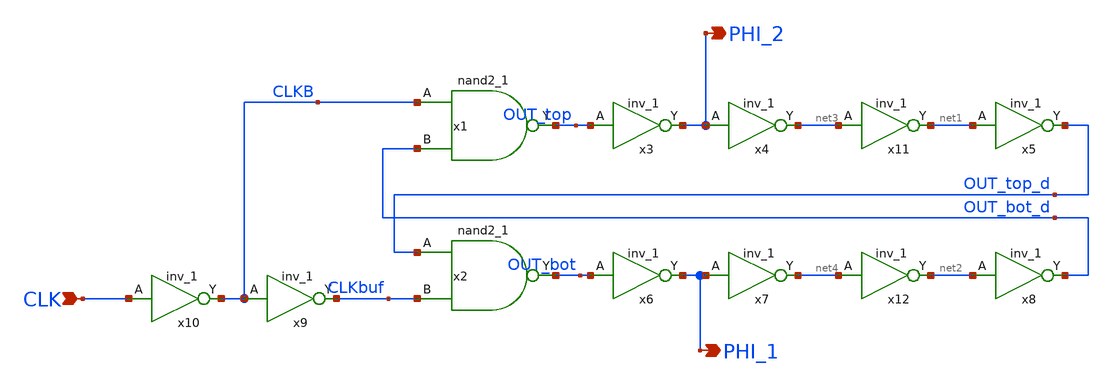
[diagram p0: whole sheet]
** sch_path: designs/switch_matrix_gf180mcu_9t5v0-main/designs/libs/core_swmatrix/NO_ClkGen.sch
**.subckt NO_ClkGen CLK PHI_2 PHI_1
*.ipin CLK
*.opin PHI_2
*.opin PHI_1
x1 CLKB OUT_bot_d VSSd VDDd VSSd VDDd OUT_top gf180mcu_fd_sc_mcu9t5v0__nand2_1
x2 OUT_top_d CLKbuf VSSd VDDd VSSd VDDd OUT_bot gf180mcu_fd_sc_mcu9t5v0__nand2_1
x3 OUT_top VSSd VDDd VSSd VDDd PHI_2 gf180mcu_fd_sc_mcu9t5v0__inv_1
x4 PHI_2 VSSd VDDd VSSd VDDd net3 gf180mcu_fd_sc_mcu9t5v0__inv_1
x5 net1 VSSd VDDd VSSd VDDd OUT_top_d gf180mcu_fd_sc_mcu9t5v0__inv_1
x6 OUT_bot VSSd VDDd VSSd VDDd PHI_1 gf180mcu_fd_sc_mcu9t5v0__inv_1
x7 PHI_1 VSSd VDDd VSSd VDDd net4 gf180mcu_fd_sc_mcu9t5v0__inv_1
x8 net2 VSSd VDDd VSSd VDDd OUT_bot_d gf180mcu_fd_sc_mcu9t5v0__inv_1
x9 CLKB VSSd VDDd VSSd VDDd CLKbuf gf180mcu_fd_sc_mcu9t5v0__inv_1
x10 CLK VSSd VDDd VSSd VDDd CLKB gf180mcu_fd_sc_mcu9t5v0__inv_1
x11 net3 VSSd VDDd VSSd VDDd net1 gf180mcu_fd_sc_mcu9t5v0__inv_1
x12 net4 VSSd VDDd VSSd VDDd net2 gf180mcu_fd_sc_mcu9t5v0__inv_1
**.ends
.end
